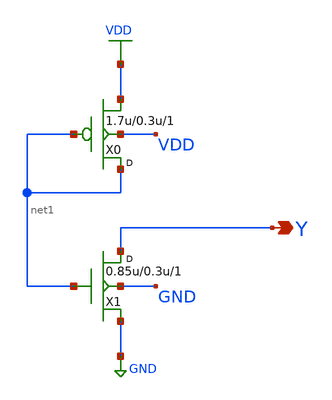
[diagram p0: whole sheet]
** sch_path: lib/xschem/gf180mcu_osu_sc_12T_tielo.sch
**.subckt gf180mcu_osu_sc_12T_tielo Y
*.opin Y
X0 net1 net1 VDD VDD pmos_3p3 w=1.7u l=0.3u m=1
X1 Y net1 GND GND nmos_3p3 w=0.85u l=0.3u m=1
**** begin user architecture code


.inc "/import/yukari1/lrburle/OSU_180/char/techfiles/design.hspice"
.lib "/import/yukari1/lrburle/OSU_180/char/techfiles/sm141064.hspice" typical


**** end user architecture code
**.ends
.GLOBAL VDD
.GLOBAL GND
.end
